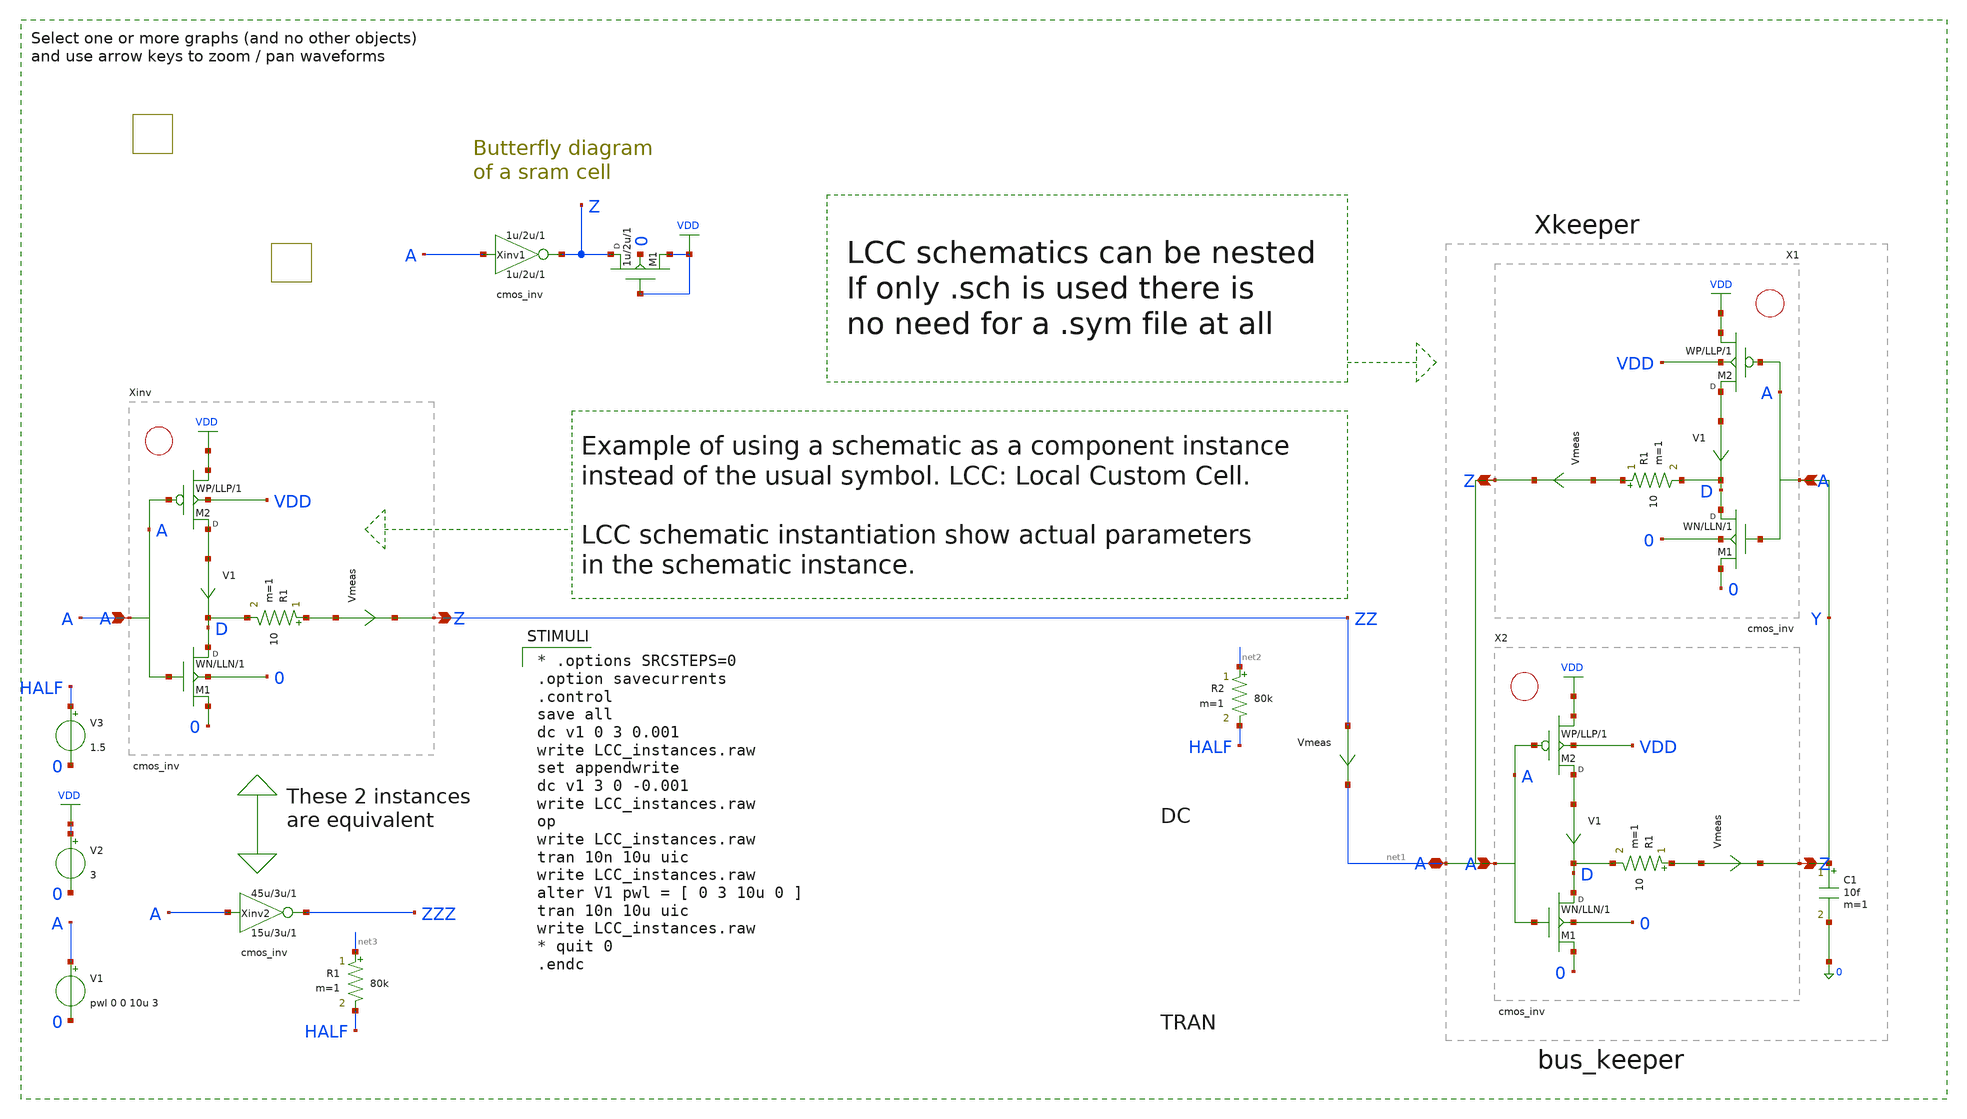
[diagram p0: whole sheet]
** sch_path: xschem_libs_newsym/examples/LCC_instances/schematic/LCC_instances.sch
* Copyright (C) 1998-2024 Stefan Frederik Schippers
* This program is free software; you can redistribute it and/or modify
* it under the terms of the GNU General Public License as published by
* the Free Software Foundation; either version 2 of the License, or
* (at your option) any later version.
* This program is distributed in the hope that it will be useful,
* but WITHOUT ANY WARRANTY; without even the implied warranty of
* MERCHANTABILITY or FITNESS FOR A PARTICULAR PURPOSE.  See the
* GNU General Public License for more details.
* You should have received a copy of the GNU General Public License
* along with this program; if not, write to the Free Software
* StefanSchippers/xschem/xschem_library/examples/cmos_inv.sch:
* Copyright (C) 1998-2023 Stefan Frederik Schippers
**.subckt LCC_instances
V1 A 0 pwl 0 0 10u 3
.save i(v1)
V2 VDD 0 3
.save i(v2)
R1 net3 HALF 80k m=1
V3 HALF 0 1.5
.save i(v3)
R2 net2 HALF 80k m=1
Xinv ZZ A cmos_inv WN=15u WP=45u LLN=3u LLP=3u m=1
Xinv2 ZZZ A cmos_inv WN=15u WP=45u LLN=3u LLP=3u m=1
Xkeeper net1 bus_keeper WN_FB=6u WP_FB=12u
Xinv1 Z A cmos_inv WN=1u WP=1u LLN=2u LLP=2u m=1
Vmeas ZZ net1 0
.save i(vmeas)
M1 Z VDD VDD 0 n w=1u l=2u m=1
**** begin user architecture code

* .options SRCSTEPS=0
.option savecurrents
.control
save all
dc v1 0 3 0.001
write LCC_instances.raw
set appendwrite
dc v1 3 0 -0.001
write LCC_instances.raw
op
write LCC_instances.raw
tran 10n 10u uic
write LCC_instances.raw
alter V1 pwl = [ 0 3 10u 0 ]
tran 10n 10u uic
write LCC_instances.raw
* quit 0
.endc



************************************************
*         NOMINAL N-Channel Transistor         *
*            UCB-3 Parameter Set               *
*         HIGH-SPEED CMOS Logic Family         *
*                10-Jan.-1995                  *
************************************************
.Model N NMOS ( LEVEL = 3 KP    = 45.3E-6 VTO   = 0.72 TOX   = 51.5E-9 NSUB  = 2.8E15 GAMMA = 0.94
+ PHI   = 0.65 VMAX  = 150E3 RS    = 40 RD    = 40 XJ    = 0.11E-6 LD    = 0.52E-6 DELTA = 0.315 THETA =
+ 0.054 ETA   = 0.025 KAPPA = 0.0 WD    = 0.0 )

***********************************************
*        NOMINAL P-Channel transistor         *
*           UCB-3 Parameter Set               *
*         HIGH-SPEED CMOS Logic Family        *
*               10-Jan.-1995                  *
***********************************************
.Model P PMOS ( LEVEL = 3 KP    = 22.1E-6 VTO   = -0.71 TOX   = 51.5E-9 NSUB  = 3.3E16 GAMMA = 0.92
+ PHI   = 0.65 VMAX  = 970E3 RS    = 80 RD    = 80 XJ    = 0.63E-6 LD    = 0.23E-6 DELTA = 2.24 THETA =
+ 0.108 ETA   = 0.322 KAPPA = 0.0 WD    = 0.0 )





**** end user architecture code
**.ends

* expanding   symbol:  examples/cmos_inv.sch # of pins=2
** sym_path: examples/cmos_inv.sch
** sch_path: examples/cmos_inv.sch
.subckt cmos_inv Z A  WN=15u WP=45u LLN=3u LLP=3u
*.opin Z
*.ipin A
M2 net1 A VDD VDD p w=WP l=LLP m=1
M1 D A 0 0 n w=WN l=LLN m=1
R1 net2 D 10 m=1
V1 net1 D 0
.save i(v1)
Vmeas net2 Z 0
.save i(vmeas)
.ends


* expanding   symbol:  examples/bus_keeper.sch # of pins=1
** sym_path: xschem_library_oa/examples/bus_keeper/schematic/bus_keeper.sch
** sch_path: xschem_library_oa/examples/bus_keeper/schematic/bus_keeper.sch
.subckt bus_keeper A  WN_FB=1u WP_FB=2u
*.iopin A
X2 Y A cmos_inv WN=15u WP=45u LLN=3u LLP=3u m=1
X1 A Y cmos_inv WN=WN_FB WP=WP_FB LLN=3u LLP=3u m=1
C1 Y 0 10f m=1
.ends

.GLOBAL VDD
.end
